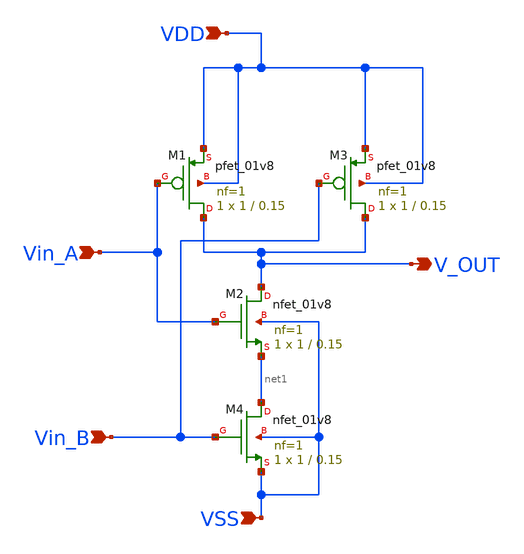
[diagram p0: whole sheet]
** sch_path: schematics_xschem/NAND.sch
**.subckt NAND Vin_A V_OUT Vin_B VSS VDD
*.ipin Vin_A
*.opin V_OUT
*.ipin Vin_B
*.ipin VSS
*.ipin VDD
XM1 V_OUT Vin_A VDD VDD sky130_fd_pr__pfet_01v8 L=0.15 W=1 nf=1 ad='int((nf+1)/2) * W/nf * 0.29' as='int((nf+2)/2) * W/nf * 0.29'
+ pd='2*int((nf+1)/2) * (W/nf + 0.29)' ps='2*int((nf+2)/2) * (W/nf + 0.29)' nrd='0.29 / W' nrs='0.29 / W'
+ sa=0 sb=0 sd=0 mult=1 m=1
XM2 V_OUT Vin_A net1 VSS sky130_fd_pr__nfet_01v8 L=0.15 W=1 nf=1 ad='int((nf+1)/2) * W/nf * 0.29' as='int((nf+2)/2) * W/nf * 0.29'
+ pd='2*int((nf+1)/2) * (W/nf + 0.29)' ps='2*int((nf+2)/2) * (W/nf + 0.29)' nrd='0.29 / W' nrs='0.29 / W'
+ sa=0 sb=0 sd=0 mult=1 m=1
XM3 V_OUT Vin_B VDD VDD sky130_fd_pr__pfet_01v8 L=0.15 W=1 nf=1 ad='int((nf+1)/2) * W/nf * 0.29' as='int((nf+2)/2) * W/nf * 0.29'
+ pd='2*int((nf+1)/2) * (W/nf + 0.29)' ps='2*int((nf+2)/2) * (W/nf + 0.29)' nrd='0.29 / W' nrs='0.29 / W'
+ sa=0 sb=0 sd=0 mult=1 m=1
XM4 net1 Vin_B VSS VSS sky130_fd_pr__nfet_01v8 L=0.15 W=1 nf=1 ad='int((nf+1)/2) * W/nf * 0.29' as='int((nf+2)/2) * W/nf * 0.29'
+ pd='2*int((nf+1)/2) * (W/nf + 0.29)' ps='2*int((nf+2)/2) * (W/nf + 0.29)' nrd='0.29 / W' nrs='0.29 / W'
+ sa=0 sb=0 sd=0 mult=1 m=1
**.ends
.end
